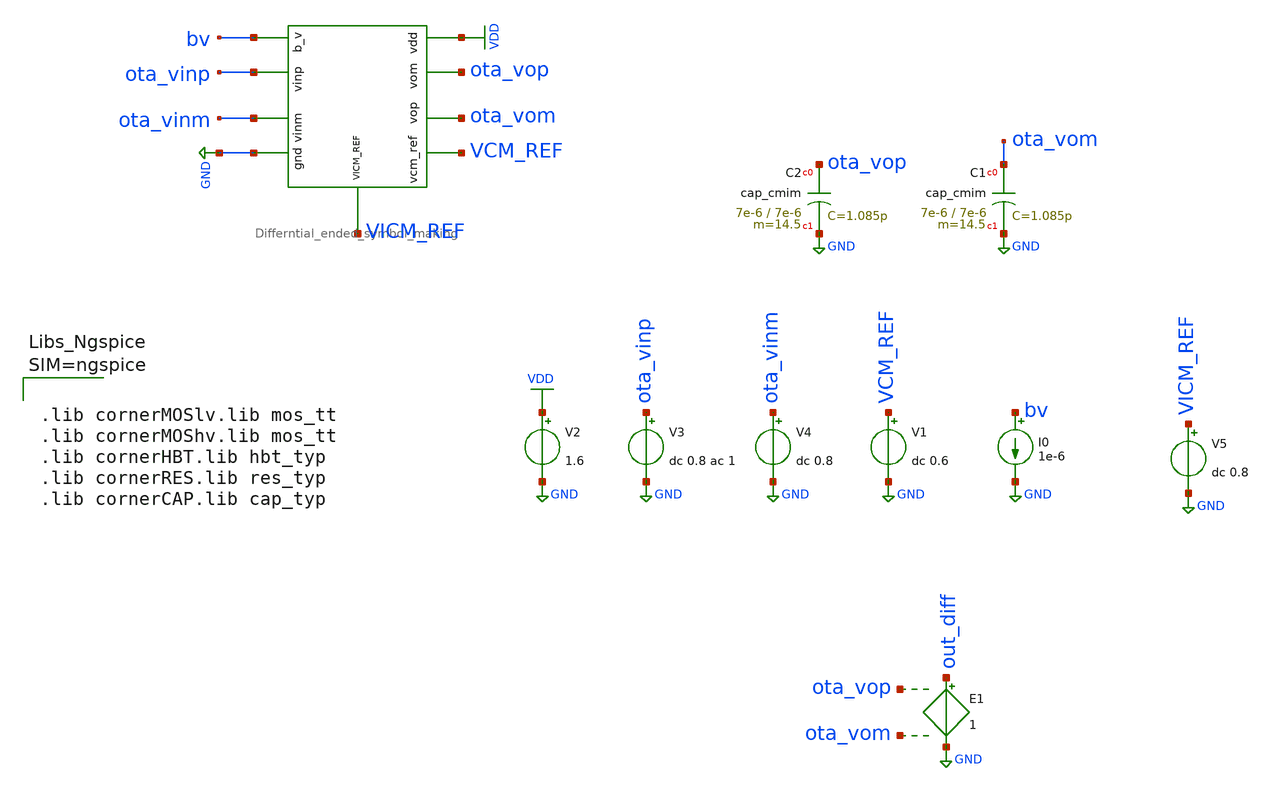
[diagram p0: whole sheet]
** sch_path: tb_ota.sch
**.subckt tb_ota
V2 VDD GND 1.6
V3 ota_vinp GND dc 0.8 ac 1
V4 ota_vinm GND dc 0.8
V1 VCM_REF GND dc 0.6
I0 bv GND 1e-6
x2 VDD VCM_REF ota_vop ota_vom GND bv ota_vinm ota_vinp VICM_REF Differntial_ended_symbol_making
V5 VICM_REF GND dc 0.8
XC1 ota_vom GND cap_cmim w=7e-6 l=7e-6 m=14.5 mm_ok=1
XC2 ota_vop GND cap_cmim w=7e-6 l=7e-6 m=14.5 mm_ok=1
E1 out_diff GND ota_vop ota_vom 1
**** begin user architecture code



.lib cornerMOSlv.lib mos_tt
.lib cornerMOShv.lib mos_tt
.lib cornerHBT.lib hbt_typ
.lib cornerRES.lib res_typ
.lib cornerCAP.lib cap_typ







.ac dec 10 100 10e8
*.save all
*.op

*.noise v(out_diff) v3 dec 10 1 10e9




**** end user architecture code
**.ends

* expanding   symbol:
*+  /home/designer/shared/uni_cass/LAST_DESIGN_FILES/Differntial_ended_symbol_making.sym # of pins=9
** sym_path: Differntial_ended_symbol_making.sym
** sch_path: Differntial_ended_symbol_making.sch
.subckt Differntial_ended_symbol_making vdd vcm_ref vom vop gnd b_v vinm vinp VICM_REF
*.iopin b_v
*.iopin vinm
*.iopin vcm_ref
*.iopin vinp
*.iopin vop
*.iopin vom
*.iopin gnd
*.iopin vdd
*.iopin VICM_REF
XM7 vop nbias gnd gnd sg13_hv_nmos w=2u l=2u ng=1 m=2 mm_ok=1
XM8 vop vinm tail vdd sg13_hv_pmos w=4.5u l=1u ng=1 m=2 mm_ok=1
XM9 vom nbias gnd gnd sg13_hv_nmos w=2u l=2u ng=1 m=2 mm_ok=1
XM10 vom vinp tail vdd sg13_hv_pmos w=4.5u l=1u ng=1 m=2 mm_ok=1
XM11 tail b_v vdd vdd sg13_hv_pmos w=4u l=1u ng=1 m=4 mm_ok=1
XM6 net1 net1 gnd gnd sg13_hv_nmos w=1u l=0.5u ng=1 m=1 mm_ok=1
XM13 net1 vop tail_cmfb vdd sg13_hv_pmos w=2.25u l=0.50u ng=1 m=1 mm_ok=1
XM14 nbias net1 gnd gnd sg13_hv_nmos w=1u l=0.5u ng=1 m=1 mm_ok=1
XM15 nbias vcm_ref tail_cmfb vdd sg13_hv_pmos w=2.25u l=0.5u ng=1 m=2 mm_ok=1
XM16 tail_cmfb b_v vdd vdd sg13_hv_pmos w=4u l=1u ng=1 m=4 mm_ok=1
XM17 net1 vom tail_cmfb vdd sg13_hv_pmos w=2.25u l=0.50u ng=1 m=1 mm_ok=1
XM1 b_v b_v vdd vdd sg13_hv_pmos w=4u l=1u ng=1 m=1 mm_ok=1
XC1 nbias gnd cap_cmim w=14.0e-6 l=50.0e-6 m=1 mm_ok=1
XM2 VICM_REF vinm vinm vdd sg13_hv_pmos w=50u l=1u ng=5 m=1 mm_ok=1
XM3 VICM_REF vinp vinp vdd sg13_hv_pmos w=50u l=1u ng=5 m=1 mm_ok=1
XM4 vdd vdd vdd vdd sg13_hv_pmos w=4.5u l=0.4u ng=1 m=4 mm_ok=1
XM5 gnd gnd gnd gnd sg13_hv_nmos w=2u l=2u ng=1 m=4 mm_ok=1
.ends

.GLOBAL GND
.GLOBAL VDD
.end
